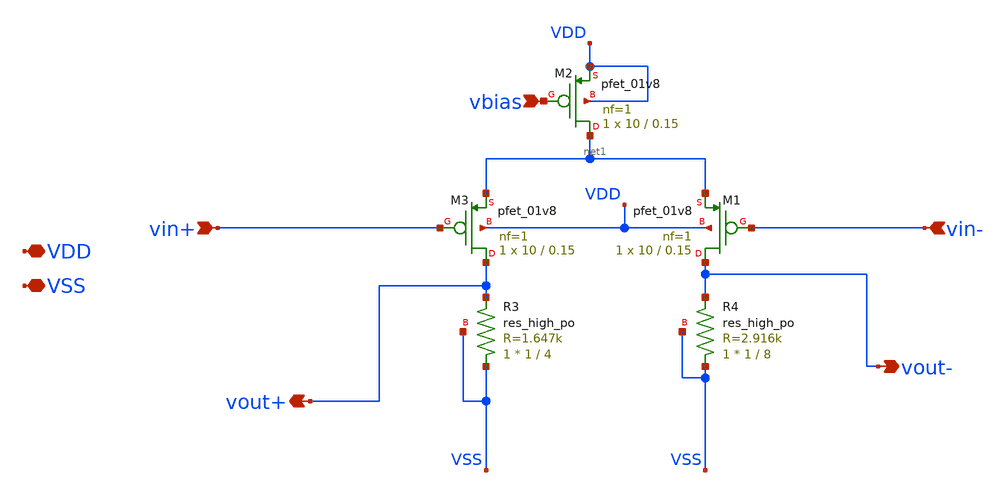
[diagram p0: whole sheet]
** sch_path: xschem/attic/LA_Limiter.sch
**.subckt LA_Limiter VDD VSS vin+ vin- vout- vout+ vbias
*.iopin VDD
*.iopin VSS
*.ipin vin+
*.ipin vin-
*.opin vout-
*.opin vout+
*.ipin vbias
XM3 vout+ vin+ net1 VDD sky130_fd_pr__pfet_01v8 L=0.15 W=10 nf=1 ad='int((nf+1)/2) * W/nf * 0.29' as='int((nf+2)/2) * W/nf * 0.29'
+ pd='2*int((nf+1)/2) * (W/nf + 0.29)' ps='2*int((nf+2)/2) * (W/nf + 0.29)' nrd='0.29 / W' nrs='0.29 / W'
+ sa=0 sb=0 sd=0 mult=1 m=1
XR3 VSS vout+ VSS sky130_fd_pr__res_high_po W=1 L=4 mult=1 m=1
XR4 VSS vout- VSS sky130_fd_pr__res_high_po W=1 L=8 mult=1 m=1
XM1 vout- vin- net1 VDD sky130_fd_pr__pfet_01v8 L=0.15 W=10 nf=1 ad='int((nf+1)/2) * W/nf * 0.29' as='int((nf+2)/2) * W/nf * 0.29'
+ pd='2*int((nf+1)/2) * (W/nf + 0.29)' ps='2*int((nf+2)/2) * (W/nf + 0.29)' nrd='0.29 / W' nrs='0.29 / W'
+ sa=0 sb=0 sd=0 mult=1 m=1
XM2 net1 vbias VDD VDD sky130_fd_pr__pfet_01v8 L=0.15 W=10 nf=1 ad='int((nf+1)/2) * W/nf * 0.29' as='int((nf+2)/2) * W/nf * 0.29'
+ pd='2*int((nf+1)/2) * (W/nf + 0.29)' ps='2*int((nf+2)/2) * (W/nf + 0.29)' nrd='0.29 / W' nrs='0.29 / W'
+ sa=0 sb=0 sd=0 mult=1 m=1
**.ends
.end
